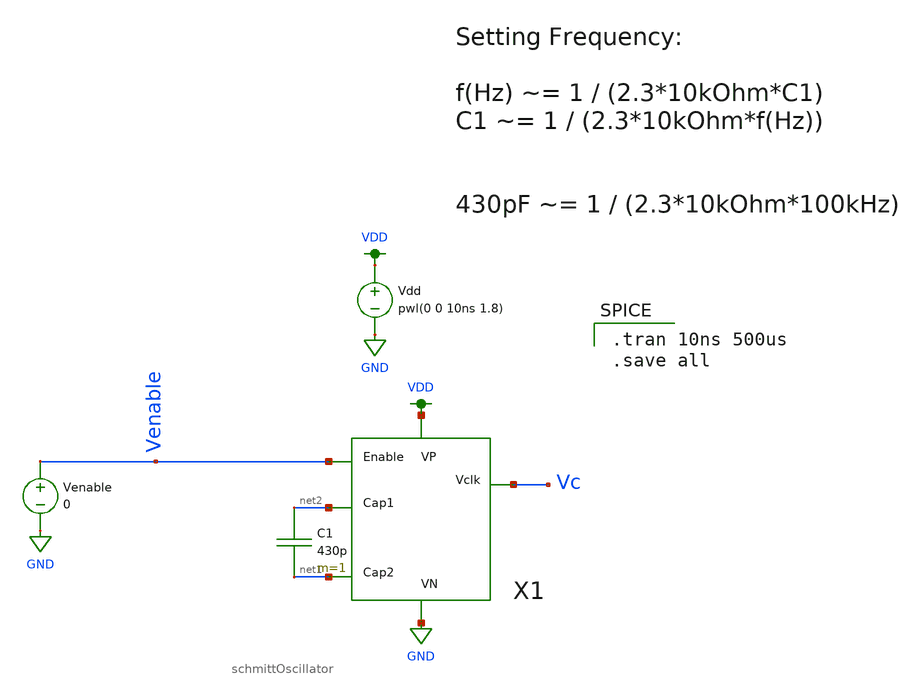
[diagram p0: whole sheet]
** sch_path: schematics/oscillatorTestbench.sch
**.subckt oscillatorTestbench
Vdd VDD GND pwl(0 0 10ns 1.8)
Venable Venable GND 0
X1 Venable net2 net1 VDD GND Vc schmittOscillator
C1 net2 net1 430p m=1
**** begin user architecture code

.option wnflag=1
.lib ~/skywater/skywater-pdk/libraries/sky130_fd_pr_ngspice/latest/models/sky130.lib.spice tt


.tran 10ns 500us
.save all

**** end user architecture code
**.ends
.GLOBAL GND
.GLOBAL VDD
.end
